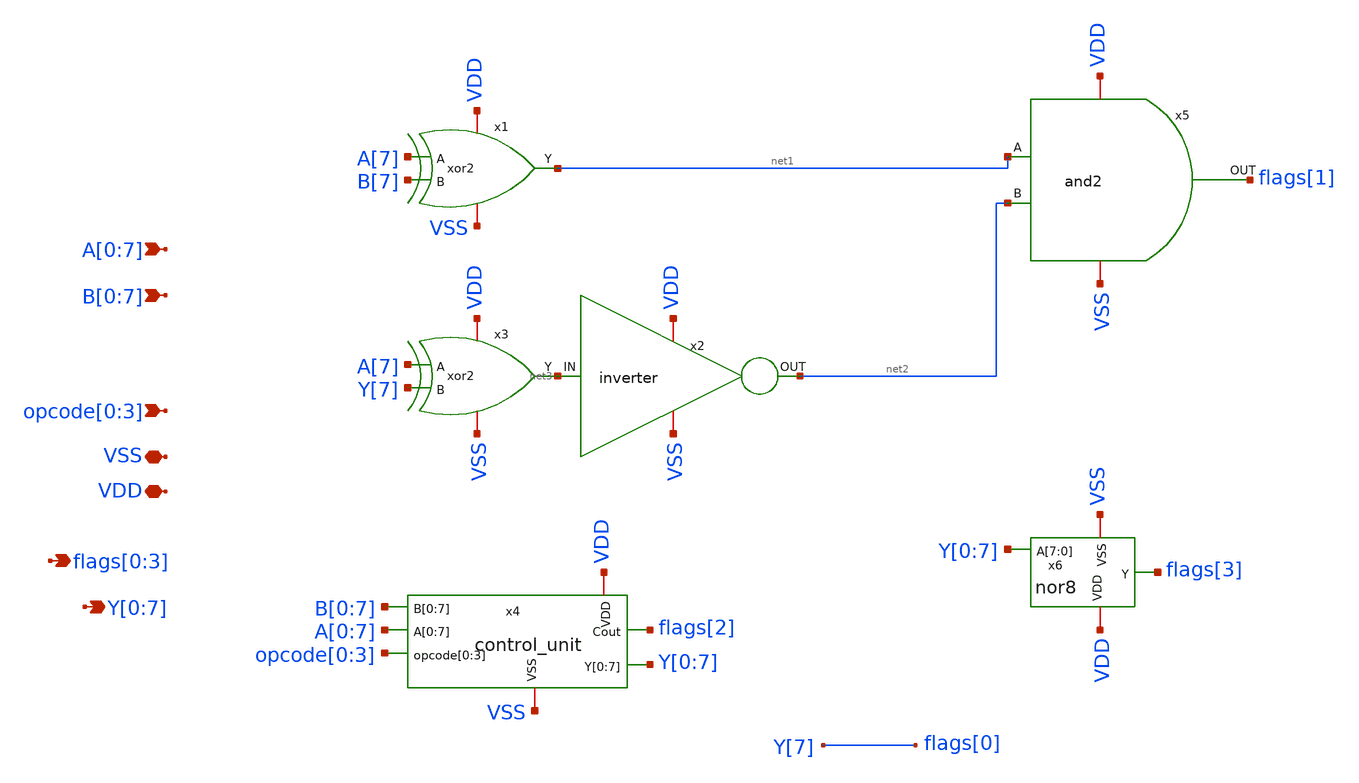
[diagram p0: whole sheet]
** sch_path: design/ALU/ALU.sch
**.subckt ALU A[0],A[1],A[2],A[3],A[4],A[5],A[6],A[7] B[0],B[1],B[2],B[3],B[4],B[5],B[6],B[7]
*+ opcode[0],opcode[1],opcode[2],opcode[3] Y[0],Y[1],Y[2],Y[3],Y[4],Y[5],Y[6],Y[7] VDD VSS flags[0],flags[1],flags[2],flags[3]
*.ipin A[0],A[1],A[2],A[3],A[4],A[5],A[6],A[7]
*.ipin B[0],B[1],B[2],B[3],B[4],B[5],B[6],B[7]
*.ipin opcode[0],opcode[1],opcode[2],opcode[3]
*.opin Y[0],Y[1],Y[2],Y[3],Y[4],Y[5],Y[6],Y[7]
*.iopin VDD
*.iopin VSS
*.opin flags[0],flags[1],flags[2],flags[3]
x1 net1 A[7] VDD VSS B[7] xor2
x2 VDD net2 net3 VSS inverter
x3 net3 A[7] VDD VSS Y[7] xor2
x4 B[0] B[1] B[2] B[3] B[4] B[5] B[6] B[7] A[0] A[1] A[2] A[3] A[4] A[5] A[6] A[7] Y[0] Y[1] Y[2]
+ Y[3] Y[4] Y[5] Y[6] Y[7] VDD VSS opcode[0] opcode[1] opcode[2] opcode[3] flags[2] control_unit
x5 VSS net1 net2 VDD flags[1] and2
x6 Y[0] Y[1] Y[2] Y[3] Y[4] Y[5] Y[6] Y[7] VSS VDD flags[3] nor8
**.ends
.end
